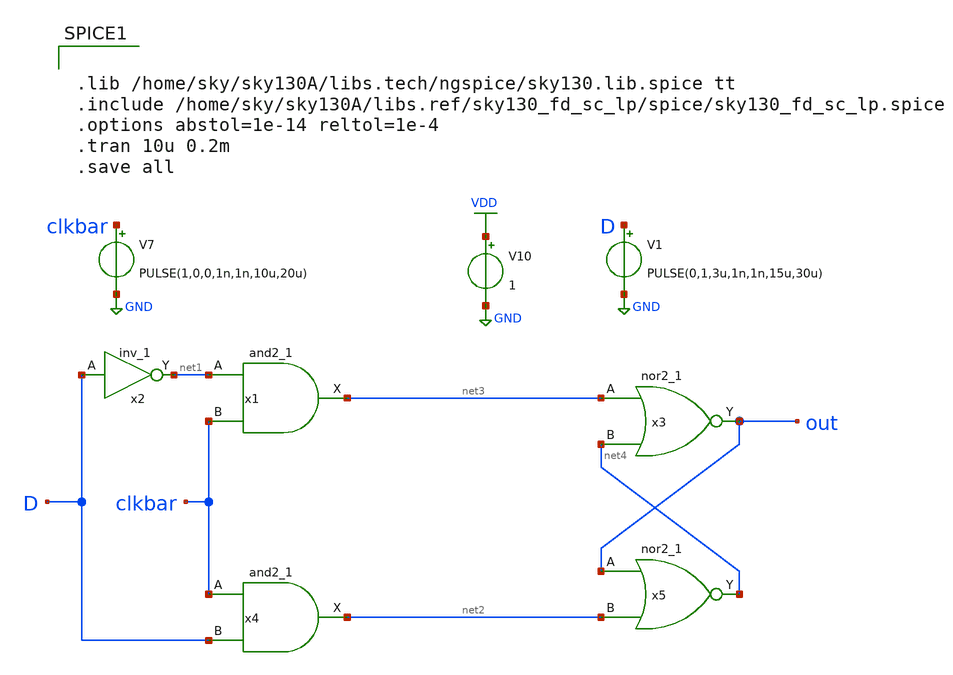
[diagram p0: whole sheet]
** sch_path: xschem/comparator/nordlatch.sch
**.subckt nordlatch
x1 net1 clkbar GND GND VDD VDD net3 sky130_fd_sc_lp__and2_1
x2 D GND GND VDD VDD net1 sky130_fd_sc_lp__inv_1
x3 net3 net4 GND GND VDD VDD out sky130_fd_sc_lp__nor2_1
x4 clkbar D GND GND VDD VDD net2 sky130_fd_sc_lp__and2_1
x5 out net2 GND GND VDD VDD net4 sky130_fd_sc_lp__nor2_1
V7 clkbar GND PULSE(1,0,0,1n,1n,10u,20u)
V10 VDD GND 1
V1 D GND PULSE(0,1,3u,1n,1n,15u,30u)
**** begin user architecture code


.lib /home/sky/sky130A/libs.tech/ngspice/sky130.lib.spice tt
.include /home/sky/sky130A/libs.ref/sky130_fd_sc_lp/spice/sky130_fd_sc_lp.spice
.options abstol=1e-14 reltol=1e-4
.tran 10u 0.2m
.save all


**** end user architecture code
**.ends
.GLOBAL VDD
.GLOBAL GND
.end
